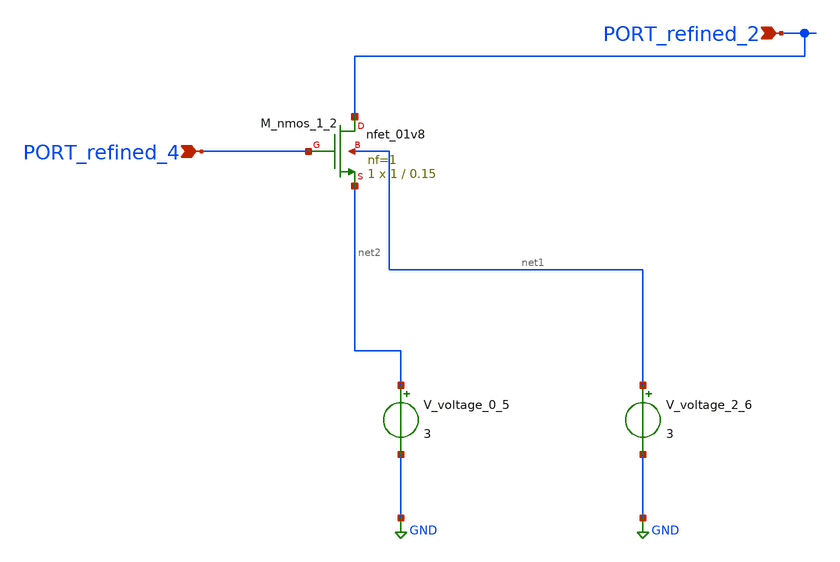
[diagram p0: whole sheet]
** sch_path: schematics/AMSNet/28.sch
**.subckt 28 PORT_refined_4 PORT_refined_2
*.ipin PORT_refined_4
*.ipin PORT_refined_2
XM_nmos_1_2 PORT_refined_2 PORT_refined_4 net2 net1 sky130_fd_pr__nfet_01v8 L=0.15 W=1 nf=1 ad='int((1 + 1)/2) * 1 / 1 * 0.29'
+ as='int((1 + 2)/2) * 1 / 1 * 0.29' pd='2*int((1 + 1)/2) * (1 / 1 + 0.29)' ps='2*int((1 + 2)/2) * (1 / 1 + 0.29)'
+ nrd='0.29 / 1 ' nrs='0.29 / 1 ' sa=0 sb=0 sd=0 mult=1 m=1
V_voltage_0_5 net2 GND 3
V_voltage_2_6 net1 GND 3
**.ends
.GLOBAL GND
.end
